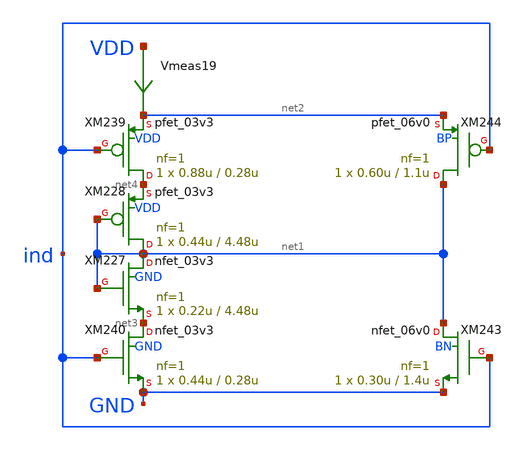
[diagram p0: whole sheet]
** sch_path: xschem_designs/sti_size5.sch
**.subckt sti_size5
XM227 net1 net1 net3 GND nfet_03v3 L=4.48u W=0.22u nf=1 ad='int((nf+1)/2) * W/nf * 0.18u' as='int((nf+2)/2) * W/nf * 0.18u'
+ pd='2*int((nf+1)/2) * (W/nf + 0.18u)' ps='2*int((nf+2)/2) * (W/nf + 0.18u)' nrd='0.18u / W' nrs='0.18u / W'
+ sa=0 sb=0 sd=0 m=1 par=1
XM228 net1 net1 net4 VDD pfet_03v3 L=4.48u W=0.44u nf=1 ad='int((nf+1)/2) * W/nf * 0.18u' as='int((nf+2)/2) * W/nf * 0.18u'
+ pd='2*int((nf+1)/2) * (W/nf + 0.18u)' ps='2*int((nf+2)/2) * (W/nf + 0.18u)' nrd='0.18u / W' nrs='0.18u / W'
+ sa=0 sb=0 sd=0 m=1 par=1
XM239 net4 ind net2 VDD pfet_03v3 L=0.28u W=0.88u nf=1 ad='int((nf+1)/2) * W/nf * 0.18u' as='int((nf+2)/2) * W/nf * 0.18u'
+ pd='2*int((nf+1)/2) * (W/nf + 0.18u)' ps='2*int((nf+2)/2) * (W/nf + 0.18u)' nrd='0.18u / W' nrs='0.18u / W'
+ sa=0 sb=0 sd=0 m=1 par=1
XM240 net3 ind GND GND nfet_03v3 L=0.28u W=0.44u nf=1 ad='int((nf+1)/2) * W/nf * 0.18u' as='int((nf+2)/2) * W/nf * 0.18u'
+ pd='2*int((nf+1)/2) * (W/nf + 0.18u)' ps='2*int((nf+2)/2) * (W/nf + 0.18u)' nrd='0.18u / W' nrs='0.18u / W'
+ sa=0 sb=0 sd=0 m=1 par=1
XM243 net1 ind GND BN nfet_06v0 L=1.4u W=0.30u nf=1 ad='int((nf+1)/2) * W/nf * 0.18u' as='int((nf+2)/2) * W/nf * 0.18u'
+ pd='2*int((nf+1)/2) * (W/nf + 0.18u)' ps='2*int((nf+2)/2) * (W/nf + 0.18u)' nrd='0.18u / W' nrs='0.18u / W'
+ sa=0 sb=0 sd=0 m=1 par=1
XM244 net1 ind net2 BP pfet_06v0 L=1.1u W=0.60u nf=1 ad='int((nf+1)/2) * W/nf * 0.18u' as='int((nf+2)/2) * W/nf * 0.18u'
+ pd='2*int((nf+1)/2) * (W/nf + 0.18u)' ps='2*int((nf+2)/2) * (W/nf + 0.18u)' nrd='0.18u / W' nrs='0.18u / W'
+ sa=0 sb=0 sd=0 m=1 par=1
Vmeas19 VDD net2 0
.save i(vmeas19)
**.ends
.end
